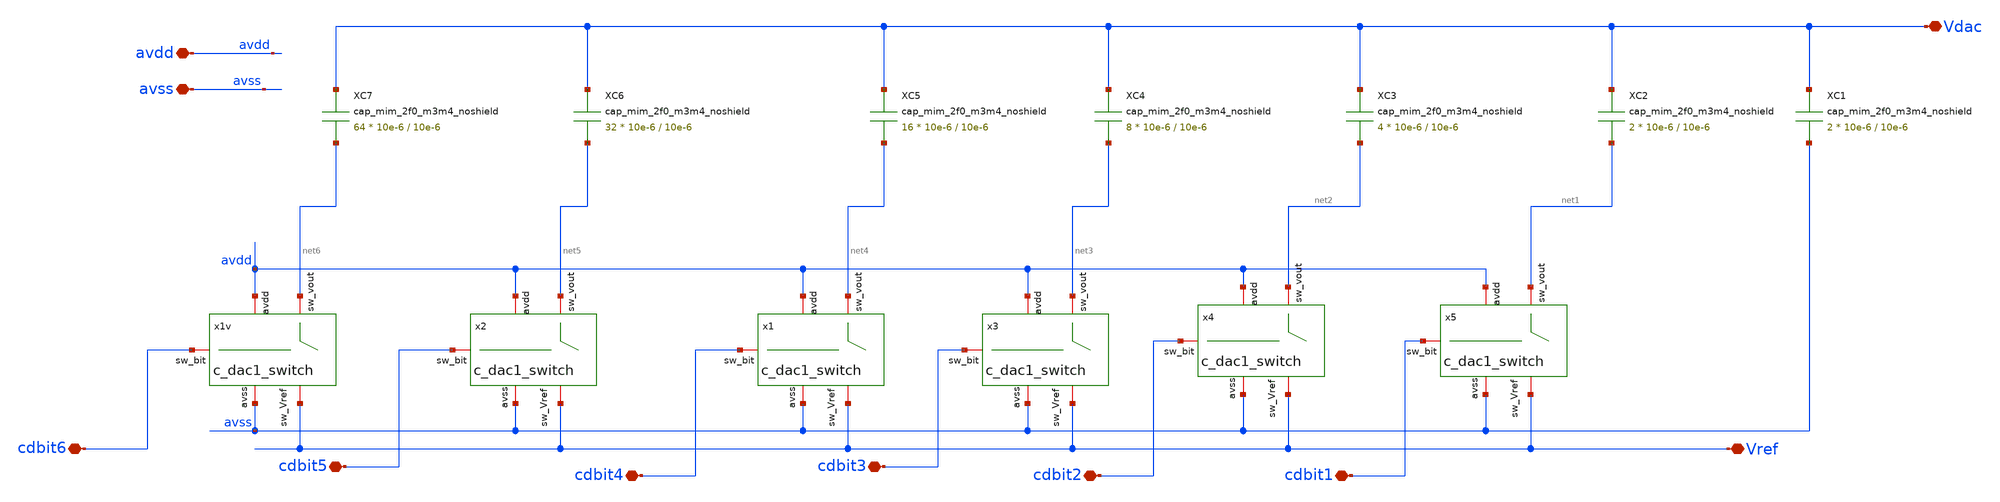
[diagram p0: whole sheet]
** sch_path: designs/libs/WK_Kadam/6bit_CDAC_CO_MK.sch
**.subckt 6bit_CDAC_CO_MK Vref Vdac avdd avss cdbit6 cdbit5 cdbit4 cdbit3 cdbit2 cdbit1
*.iopin Vref
*.iopin Vdac
*.iopin avdd
*.iopin avss
*.iopin cdbit6
*.iopin cdbit5
*.iopin cdbit4
*.iopin cdbit3
*.iopin cdbit2
*.iopin cdbit1
XC3 Vdac net2 cap_mim_2f0_m3m4_noshield c_width=10e-6 c_length=10e-6 m=4
XC4 Vdac net3 cap_mim_2f0_m3m4_noshield c_width=10e-6 c_length=10e-6 m=8
XC5 Vdac net4 cap_mim_2f0_m3m4_noshield c_width=10e-6 c_length=10e-6 m=16
XC6 Vdac net5 cap_mim_2f0_m3m4_noshield c_width=10e-6 c_length=10e-6 m=32
XC7 Vdac net6 cap_mim_2f0_m3m4_noshield c_width=10e-6 c_length=10e-6 m=64
XC1 Vdac avss cap_mim_2f0_m3m4_noshield c_width=10e-6 c_length=10e-6 m=2
XC2 Vdac net1 cap_mim_2f0_m3m4_noshield c_width=10e-6 c_length=10e-6 m=2
x1v avdd avss net6 cdbit6 Vref c_dac1_switch
x2 avdd avss net5 cdbit5 Vref c_dac1_switch
x1 avdd avss net4 cdbit4 Vref c_dac1_switch
x3 avdd avss net3 cdbit3 Vref c_dac1_switch
x4 avdd avss net2 cdbit2 Vref c_dac1_switch
x5 avdd avss net1 cdbit1 Vref c_dac1_switch
**.ends

* expanding   symbol:  Wk_Chip_Odyssey/designs/libs/WK_Kadam/c_dac1_switch.sym # of pins=5
** sym_path: designs/libs/WK_Kadam/c_dac1_switch.sym
** sch_path: designs/libs/WK_Kadam/c_dac1_switch.sch
.subckt c_dac1_switch avdd avss sw_vout sw_bit sw_Vref
*.iopin avdd
*.iopin avss
*.iopin sw_bit
*.iopin sw_vout
*.iopin sw_Vref
XM1 sw_vout sw_bit sw_Vref avss nfet_03v3 L=0.28u W=2u nf=1 ad='int((nf+1)/2) * W/nf * 0.18u' as='int((nf+2)/2) * W/nf * 0.18u'
+ pd='2*int((nf+1)/2) * (W/nf + 0.18u)' ps='2*int((nf+2)/2) * (W/nf + 0.18u)' nrd='0.18u / W' nrs='0.18u / W'
+ sa=0 sb=0 sd=0 m=1
XM3 sw_vout net1 avss avss nfet_03v3 L=0.28u W=2u nf=1 ad='int((nf+1)/2) * W/nf * 0.18u' as='int((nf+2)/2) * W/nf * 0.18u'
+ pd='2*int((nf+1)/2) * (W/nf + 0.18u)' ps='2*int((nf+2)/2) * (W/nf + 0.18u)' nrd='0.18u / W' nrs='0.18u / W'
+ sa=0 sb=0 sd=0 m=1
XM4 avss sw_bit sw_vout avdd pfet_03v3 L=0.28u W=2u nf=1 ad='int((nf+1)/2) * W/nf * 0.18u' as='int((nf+2)/2) * W/nf * 0.18u'
+ pd='2*int((nf+1)/2) * (W/nf + 0.18u)' ps='2*int((nf+2)/2) * (W/nf + 0.18u)' nrd='0.18u / W' nrs='0.18u / W'
+ sa=0 sb=0 sd=0 m=1
XM2 sw_Vref net1 sw_vout avdd pfet_03v3 L=0.28u W=2u nf=1 ad='int((nf+1)/2) * W/nf * 0.18u' as='int((nf+2)/2) * W/nf * 0.18u'
+ pd='2*int((nf+1)/2) * (W/nf + 0.18u)' ps='2*int((nf+2)/2) * (W/nf + 0.18u)' nrd='0.18u / W' nrs='0.18u / W'
+ sa=0 sb=0 sd=0 m=1
x1v avdd sw_bit net1 avss inv_test
.ends


* expanding   symbol:  Wk_Chip_Odyssey/designs/libs/WK_Kadam/inv_test.sym # of pins=4
** sym_path: Wk_Chip_Odyssey/designs/libs/WK_Kadam/inv_test.sym
** sch_path: Wk_Chip_Odyssey/designs/libs/WK_Kadam/inv_test.sch
.subckt inv_test avdd in out avss
*.iopin avdd
*.iopin avss
*.iopin in
*.iopin out
XM3 out in avss avss nfet_03v3 L=0.28u W=1u nf=1 ad='int((nf+1)/2) * W/nf * 0.18u' as='int((nf+2)/2) * W/nf * 0.18u'
+ pd='2*int((nf+1)/2) * (W/nf + 0.18u)' ps='2*int((nf+2)/2) * (W/nf + 0.18u)' nrd='0.18u / W' nrs='0.18u / W'
+ sa=0 sb=0 sd=0 m=1
XM4 out in avdd avdd pfet_03v3 L=0.28u W=2.5u nf=1 ad='int((nf+1)/2) * W/nf * 0.18u' as='int((nf+2)/2) * W/nf * 0.18u'
+ pd='2*int((nf+1)/2) * (W/nf + 0.18u)' ps='2*int((nf+2)/2) * (W/nf + 0.18u)' nrd='0.18u / W' nrs='0.18u / W'
+ sa=0 sb=0 sd=0 m=1
.ends

.end
